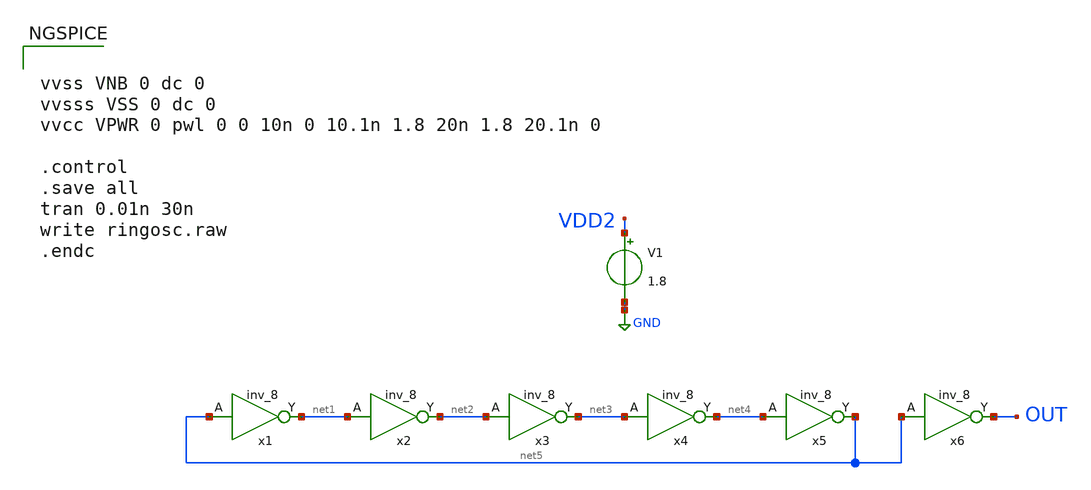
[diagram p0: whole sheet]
** sch_path: images/foss-asic-tools/addons/examples/sky130-analog/designs/ringosc/ringosc.sch
**.subckt ringosc
x1 net5 VSS VNB VPWR VPWR net1 sky130_fd_sc_hd__inv_8
x2 net1 VSS VNB VPWR VPWR net2 sky130_fd_sc_hd__inv_8
x3 net2 VSS VNB VPWR VPWR net3 sky130_fd_sc_hd__inv_8
x4 net3 VSS VNB VPWR VPWR net4 sky130_fd_sc_hd__inv_8
x5 net4 VSS VNB VPWR VPWR net5 sky130_fd_sc_hd__inv_8
x6 net5 VSS VNB VDD2 VDD2 OUT sky130_fd_sc_hd__inv_8
V1 VDD2 GND 1.8
**** begin user architecture code


vvss VNB 0 dc 0
vvsss VSS 0 dc 0
vvcc VPWR 0 pwl 0 0 10n 0 10.1n 1.8 20n 1.8 20.1n 0

.control
.save all
tran 0.01n 30n
write ringosc.raw
.endc



.include $::SKYWATER_MODELS/cells/nfet_01v8/sky130_fd_pr__nfet_01v8__tt.corner.spice
.include $::SKYWATER_MODELS/cells/nfet_01v8_lvt/sky130_fd_pr__nfet_01v8_lvt__tt.corner.spice
.include $::SKYWATER_MODELS/cells/pfet_01v8/sky130_fd_pr__pfet_01v8__tt.corner.spice
.include $::SKYWATER_MODELS/cells/nfet_03v3_nvt/sky130_fd_pr__nfet_03v3_nvt__tt.corner.spice
.include $::SKYWATER_MODELS/cells/nfet_05v0_nvt/sky130_fd_pr__nfet_05v0_nvt__tt.corner.spice
.include $::SKYWATER_MODELS/cells/esd_nfet_01v8/sky130_fd_pr__esd_nfet_01v8__tt.corner.spice
.include $::SKYWATER_MODELS/cells/pfet_01v8_lvt/sky130_fd_pr__pfet_01v8_lvt__tt.corner.spice
.include $::SKYWATER_MODELS/cells/pfet_01v8_hvt/sky130_fd_pr__pfet_01v8_hvt__tt.corner.spice
.include $::SKYWATER_MODELS/cells/esd_pfet_g5v0d10v5/sky130_fd_pr__esd_pfet_g5v0d10v5__tt.corner.spice
.include $::SKYWATER_MODELS/cells/pfet_g5v0d10v5/sky130_fd_pr__pfet_g5v0d10v5__tt.corner.spice
.include $::SKYWATER_MODELS/cells/pfet_g5v0d16v0/sky130_fd_pr__pfet_g5v0d16v0__tt.corner.spice
.include $::SKYWATER_MODELS/cells/nfet_g5v0d10v5/sky130_fd_pr__nfet_g5v0d10v5__tt.corner.spice
.include $::SKYWATER_MODELS/cells/nfet_g5v0d16v0/sky130_fd_pr__nfet_g5v0d16v0__tt_discrete.corner.spice
.include $::SKYWATER_MODELS/cells/esd_nfet_g5v0d10v5/sky130_fd_pr__esd_nfet_g5v0d10v5__tt.corner.spice
.include $::SKYWATER_MODELS/models/corners/tt/nonfet.spice
* Mismatch parameters
.include $::SKYWATER_MODELS/cells/nfet_01v8/sky130_fd_pr__nfet_01v8__mismatch.corner.spice
.include $::SKYWATER_MODELS/cells/pfet_01v8/sky130_fd_pr__pfet_01v8__mismatch.corner.spice
.include $::SKYWATER_MODELS/cells/nfet_01v8_lvt/sky130_fd_pr__nfet_01v8_lvt__mismatch.corner.spice
.include $::SKYWATER_MODELS/cells/pfet_01v8_lvt/sky130_fd_pr__pfet_01v8_lvt__mismatch.corner.spice
.include $::SKYWATER_MODELS/cells/pfet_01v8_hvt/sky130_fd_pr__pfet_01v8_hvt__mismatch.corner.spice
.include $::SKYWATER_MODELS/cells/nfet_g5v0d10v5/sky130_fd_pr__nfet_g5v0d10v5__mismatch.corner.spice
.include $::SKYWATER_MODELS/cells/pfet_g5v0d10v5/sky130_fd_pr__pfet_g5v0d10v5__mismatch.corner.spice
.include $::SKYWATER_MODELS/cells/nfet_05v0_nvt/sky130_fd_pr__nfet_05v0_nvt__mismatch.corner.spice
.include $::SKYWATER_MODELS/cells/nfet_03v3_nvt/sky130_fd_pr__nfet_03v3_nvt__mismatch.corner.spice
* Resistor$::SKYWATER_MODELS/Capacitor
.include $::SKYWATER_MODELS/models/r+c/res_typical__cap_typical.spice
.include $::SKYWATER_MODELS/models/r+c/res_typical__cap_typical__lin.spice
* Special cells
.include $::SKYWATER_MODELS/models/corners/tt/specialized_cells.spice
* All models
.include $::SKYWATER_MODELS/models/all.spice
* Corner
.include $::SKYWATER_MODELS/models/corners/tt/rf.spice

**** end user architecture code
**.ends
.GLOBAL GND
**** begin user architecture code
[sky130_models]
**** end user architecture code
.end
